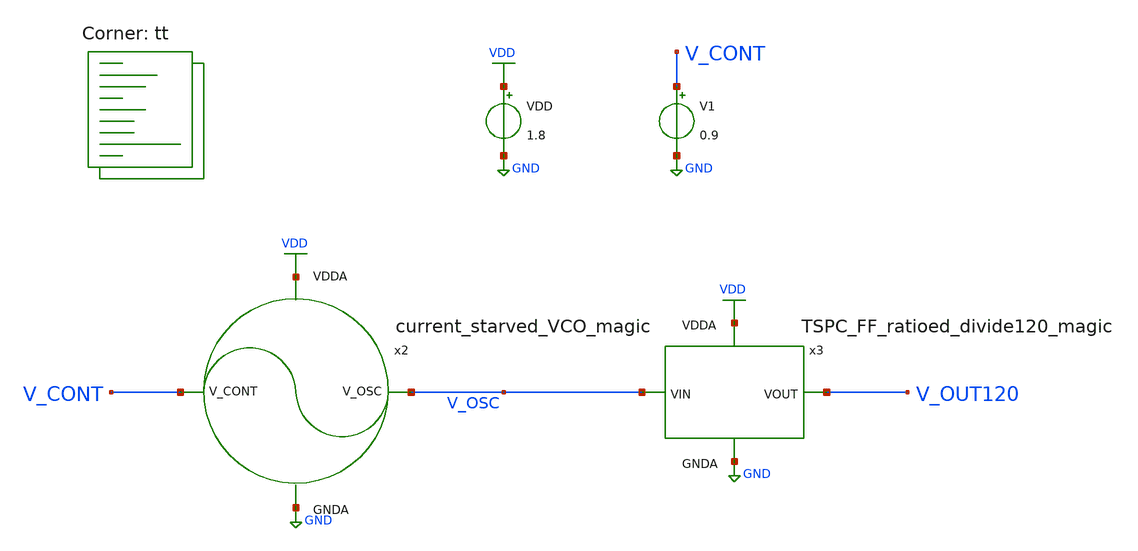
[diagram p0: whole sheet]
** sch_path: projects/pll/divider/magic/divide_by_120/tb_VCO_FD_kvco.sch
**.subckt tb_VCO_FD_kvco
VDD VDD GND 1.8
V1 V_CONT GND 0.9
x3 V_OUT120 V_OSC VDD GND TSPC_FF_ratioed_divide120_magic
x2 VDD V_OSC V_CONT GND current_starved_VCO_magic
**** begin user architecture code



.include /foss/designs/my_design/projects/pll/vco/magic/current_starved_VCO_magic.spice
.include /foss/designs/my_design/projects/pll/divider/magic/divide_by_120/TSPC_FF_ratioed_divide120_magic.spice

.option method=gear
.option wnflag=1

.control

  let v_cont_start = 0.0
  let v_cont_stop = 1.9

  dowhile v_cont_start <= v_cont_stop
    alter v1 $&v_cont_start

    save all
    * save v(v_osc)
    * save v(v_cont) v(v_osc) v(x2.v_out2) v(x2.v_out4) v(x2.v_out8) v(x2.v_out24) v(v_out120)
+  p(x1:power) p(x2:power)

    * tran 5ps 40ns
    tran 5ps 150ns

    remzerovec

    write tb_VCO_FD_kvco_{$&v_cont_start}.raw
    * write tb_VCO_FD_kvco.raw

    linearize v(v_osc)
    * linearize v(v_cont) v(v_osc) v(x2.v_out2) v(x2.v_out4) v(x2.v_out8) v(x2.v_out24) v(v_out120)

    let filename = v_cont_start * 100

    wrdata /foss/designs/my_design/projects/pll/divider/magic/divide_by_120/tb_VCO_FD_kvco_{$&filename}.txt
+ v(v_osc)
    * wrdata /foss/designs/my_design/projects/pll/divider/magic/divide_by_120/tb_VCO_FD_kvco.txt
+ v(v_osc)

    set appendwrite

    reset
    let v_cont_start = v_cont_start + 0.1
   end

.endc



.lib $::SKYWATER_MODELS/sky130.lib.spice tt
**** end user architecture code
**.ends
.GLOBAL GND
.GLOBAL VDD
.end
